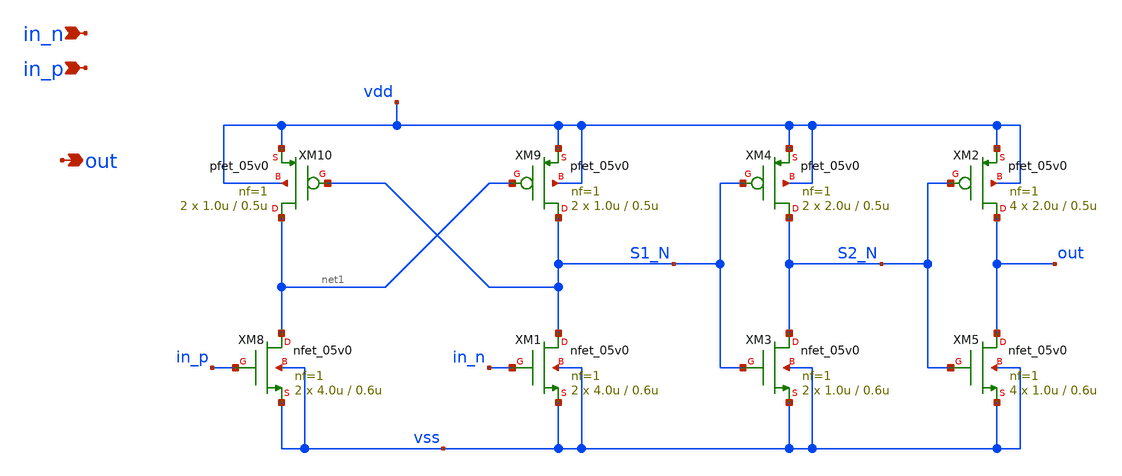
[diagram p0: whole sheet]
** sch_path: projects/programmable_transceiver_platform/analog/core_support/biasgen/xschem/level_shift_5v.sch
**.subckt level_shift_5v in_n in_p out
*.ipin in_n
*.ipin in_p
*.opin out
XM8 net1 in_p vss vss nfet_05v0 L=0.6u W=4.0u nf=1 ad='int((nf+1)/2) * W/nf * 0.18u' as='int((nf+2)/2) * W/nf * 0.18u'
+ pd='2*int((nf+1)/2) * (W/nf + 0.18u)' ps='2*int((nf+2)/2) * (W/nf + 0.18u)' nrd='0.18u / W' nrs='0.18u / W'
+ sa=0 sb=0 sd=0 m=2
XM10 net1 S1_N vdd vdd pfet_05v0 L=0.5u W=1.0u nf=1 ad='int((nf+1)/2) * W/nf * 0.18u' as='int((nf+2)/2) * W/nf * 0.18u'
+ pd='2*int((nf+1)/2) * (W/nf + 0.18u)' ps='2*int((nf+2)/2) * (W/nf + 0.18u)' nrd='0.18u / W' nrs='0.18u / W'
+ sa=0 sb=0 sd=0 m=2 par=2
XM2 out S2_N vdd vdd pfet_05v0 L=0.5u W=2.0u nf=1 ad='int((nf+1)/2) * W/nf * 0.18u' as='int((nf+2)/2) * W/nf * 0.18u'
+ pd='2*int((nf+1)/2) * (W/nf + 0.18u)' ps='2*int((nf+2)/2) * (W/nf + 0.18u)' nrd='0.18u / W' nrs='0.18u / W'
+ sa=0 sb=0 sd=0 m=4 par=4
XM9 S1_N net1 vdd vdd pfet_05v0 L=0.5u W=1.0u nf=1 ad='int((nf+1)/2) * W/nf * 0.18u' as='int((nf+2)/2) * W/nf * 0.18u'
+ pd='2*int((nf+1)/2) * (W/nf + 0.18u)' ps='2*int((nf+2)/2) * (W/nf + 0.18u)' nrd='0.18u / W' nrs='0.18u / W'
+ sa=0 sb=0 sd=0 m=2 par=2
XM4 S2_N S1_N vdd vdd pfet_05v0 L=0.5u W=2.0u nf=1 ad='int((nf+1)/2) * W/nf * 0.18u' as='int((nf+2)/2) * W/nf * 0.18u'
+ pd='2*int((nf+1)/2) * (W/nf + 0.18u)' ps='2*int((nf+2)/2) * (W/nf + 0.18u)' nrd='0.18u / W' nrs='0.18u / W'
+ sa=0 sb=0 sd=0 m=2 par=2
XM1 S1_N in_n vss vss nfet_05v0 L=0.6u W=4.0u nf=1 ad='int((nf+1)/2) * W/nf * 0.18u' as='int((nf+2)/2) * W/nf * 0.18u'
+ pd='2*int((nf+1)/2) * (W/nf + 0.18u)' ps='2*int((nf+2)/2) * (W/nf + 0.18u)' nrd='0.18u / W' nrs='0.18u / W'
+ sa=0 sb=0 sd=0 m=2
XM3 S2_N S1_N vss vss nfet_05v0 L=0.6u W=1.0u nf=1 ad='int((nf+1)/2) * W/nf * 0.18u' as='int((nf+2)/2) * W/nf * 0.18u'
+ pd='2*int((nf+1)/2) * (W/nf + 0.18u)' ps='2*int((nf+2)/2) * (W/nf + 0.18u)' nrd='0.18u / W' nrs='0.18u / W'
+ sa=0 sb=0 sd=0 m=2
XM5 out S2_N vss vss nfet_05v0 L=0.6u W=1.0u nf=1 ad='int((nf+1)/2) * W/nf * 0.18u' as='int((nf+2)/2) * W/nf * 0.18u'
+ pd='2*int((nf+1)/2) * (W/nf + 0.18u)' ps='2*int((nf+2)/2) * (W/nf + 0.18u)' nrd='0.18u / W' nrs='0.18u / W'
+ sa=0 sb=0 sd=0 m=4
**.ends
.end
